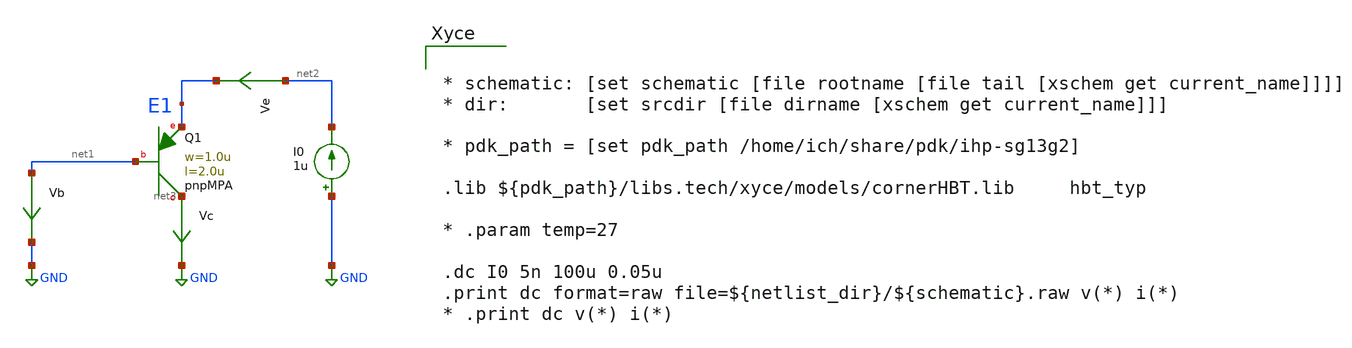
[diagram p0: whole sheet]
** sch_path: BG/design_data/xschem/simulations/dc_pnpMPA_print_raw.sch
* Copyright 2023 IHP PDK Authors
**.subckt dc_pnpMPA_print_raw
XQ1 net3 net1 E1 pnpMPA a=2p p=6u m=1
Ve net2 E1 0
.save i(ve)
Vb net1 GND 0
.save i(vb)
Vc net3 GND 0
.save i(vc)
I0 GND net2 1u
**** begin user architecture code


* schematic: [set schematic [file rootname [file tail [xschem get current_name]]]]
* dir:       [set srcdir [file dirname [xschem get current_name]]]

* pdk_path = [set pdk_path /home/ich/share/pdk/ihp-sg13g2]

.lib ${pdk_path}/libs.tech/xyce/models/cornerHBT.lib     hbt_typ

* .param temp=27

.dc I0 5n 100u 0.05u
.print dc format=raw file=${netlist_dir}/${schematic}.raw v(*) i(*)
* .print dc v(*) i(*)



**** end user architecture code
**.ends
.GLOBAL GND
.end
